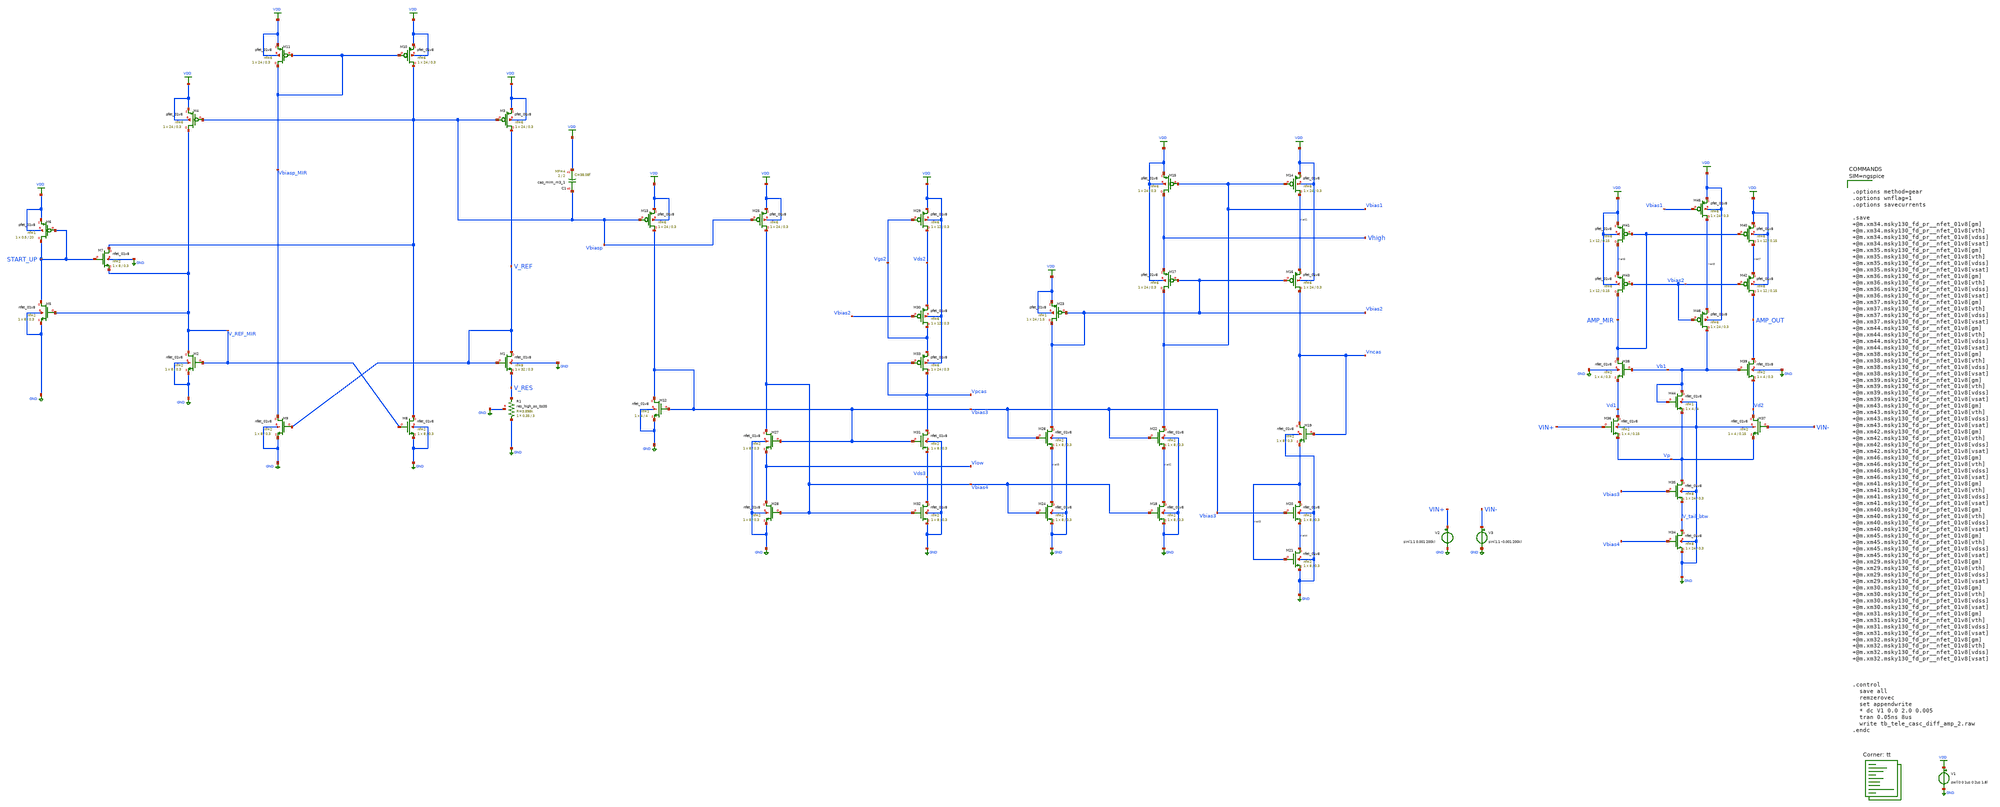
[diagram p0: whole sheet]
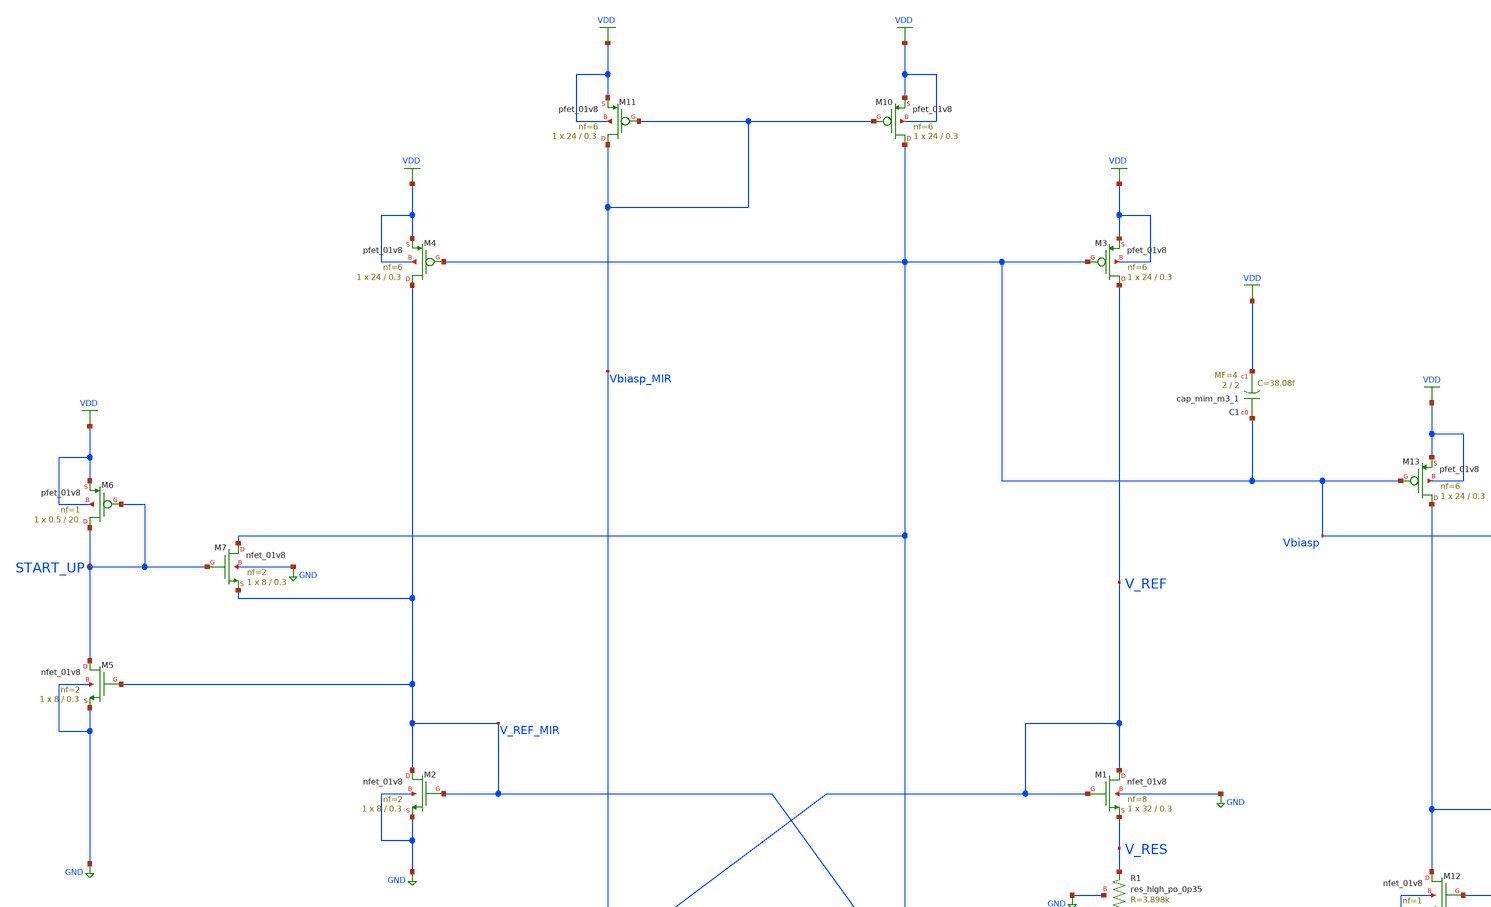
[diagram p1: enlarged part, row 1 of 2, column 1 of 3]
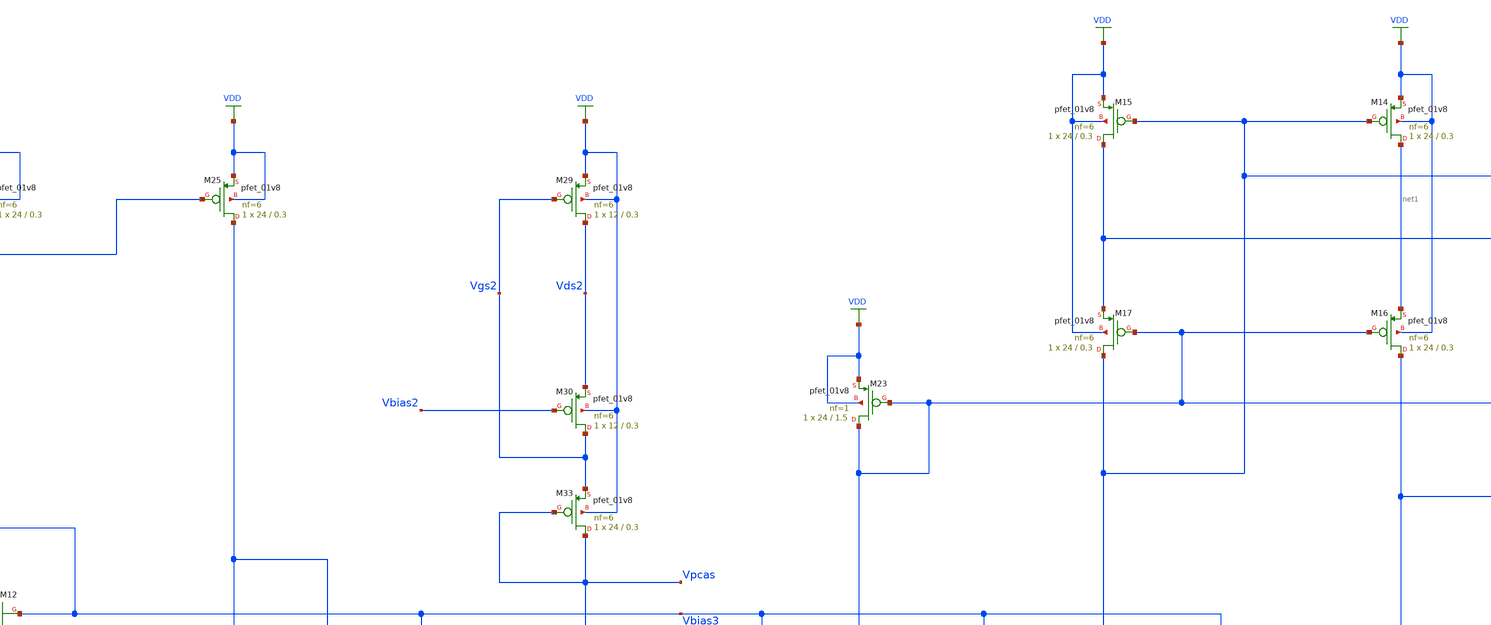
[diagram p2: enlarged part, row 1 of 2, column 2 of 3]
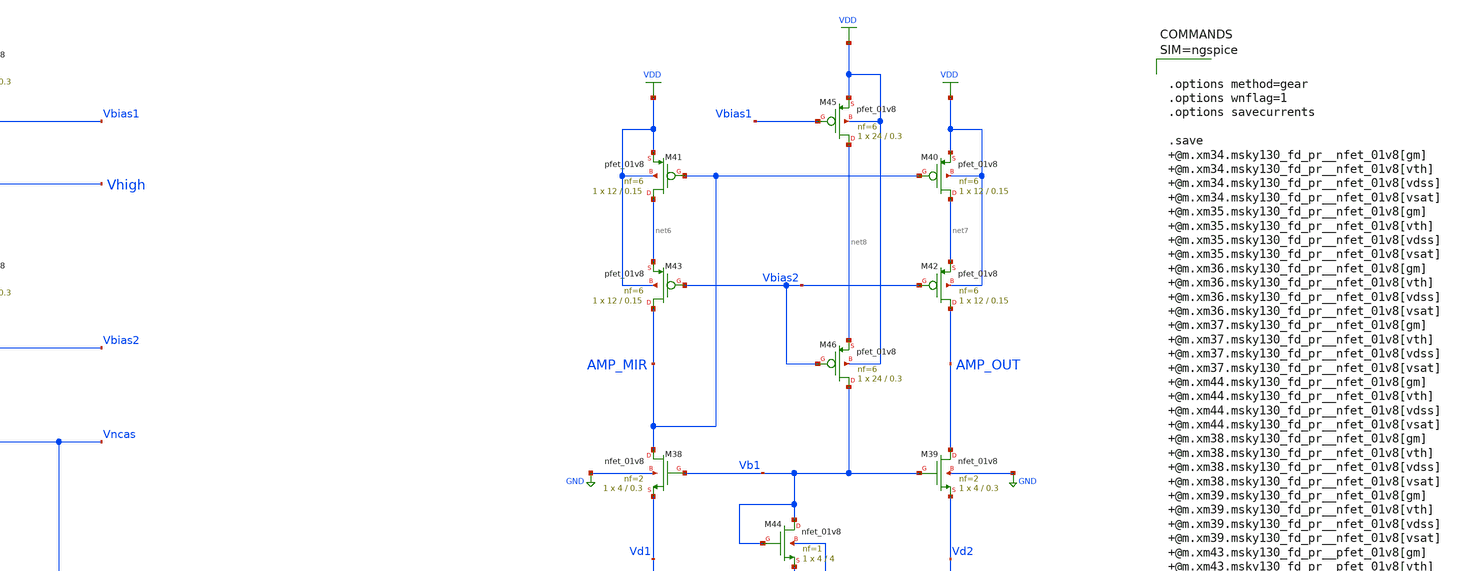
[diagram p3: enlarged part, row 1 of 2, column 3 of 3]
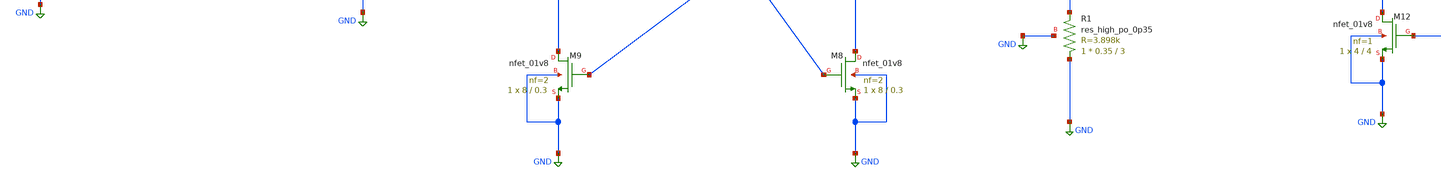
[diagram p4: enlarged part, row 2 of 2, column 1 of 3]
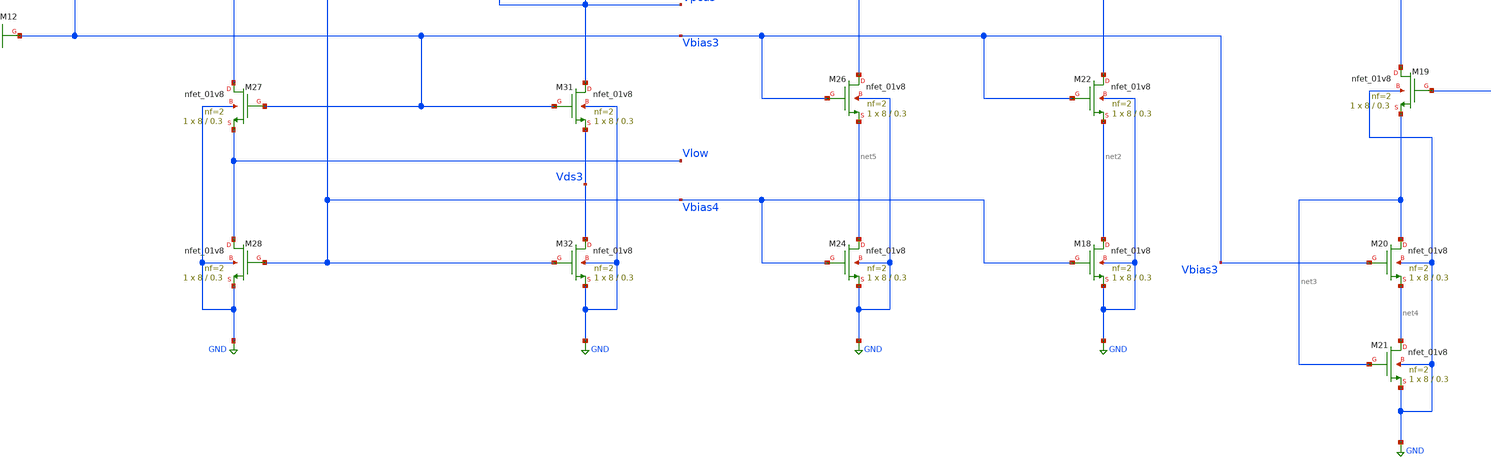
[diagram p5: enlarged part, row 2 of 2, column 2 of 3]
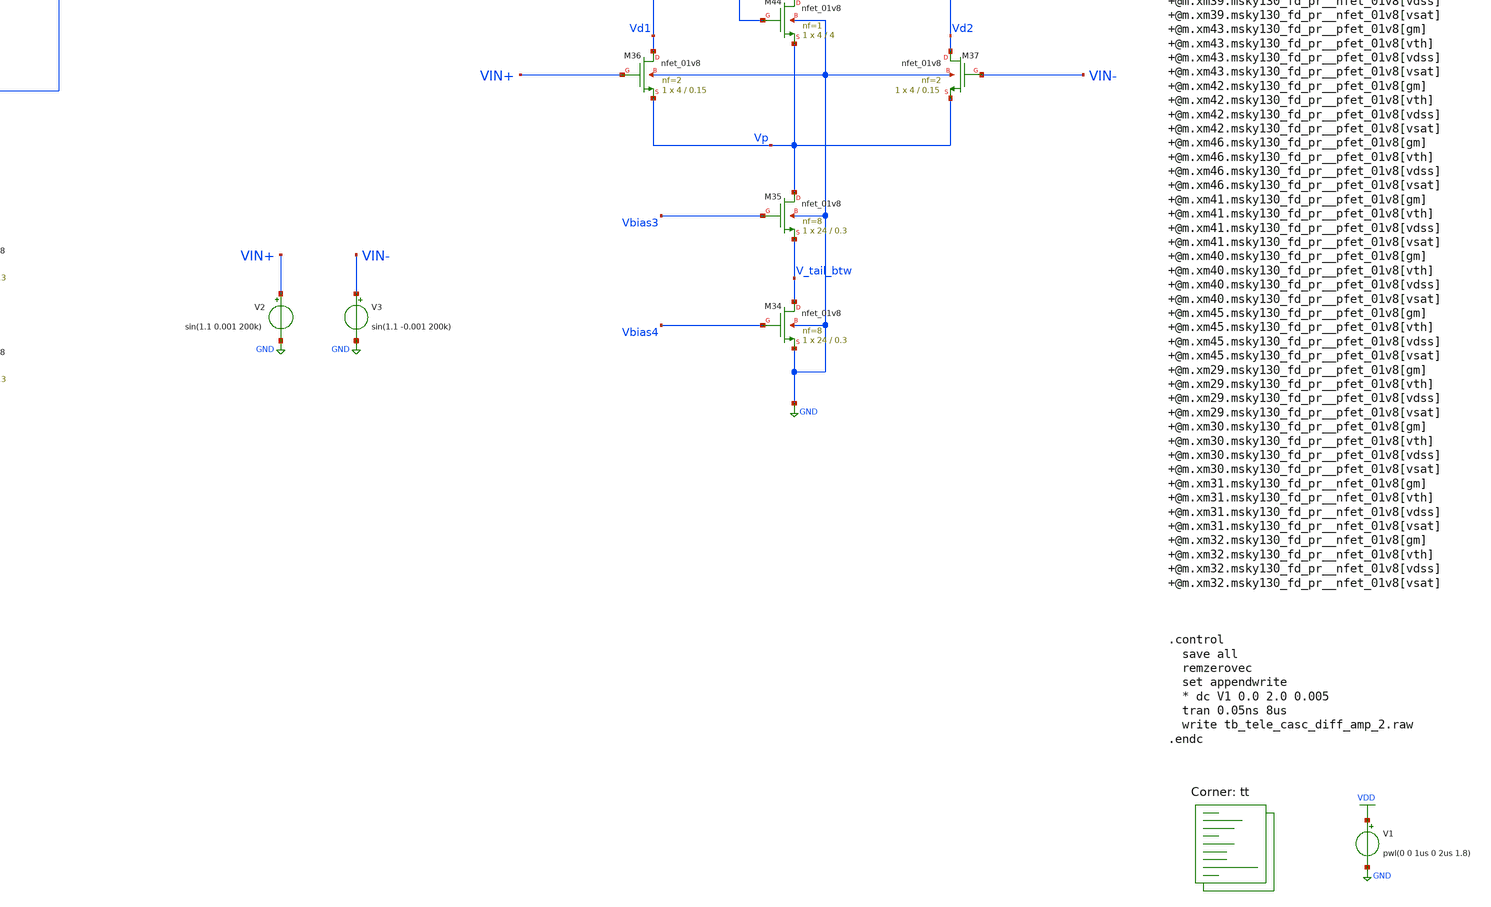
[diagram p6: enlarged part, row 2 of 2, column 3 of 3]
** sch_path: projects/ASU/EEE572/schematic/tb_tele_casc_diff_amp_2.sch
**.subckt tb_tele_casc_diff_amp_2
V1 VDD GND pwl(0 0 1us 0 2us 1.8)
XM1 V_REF V_REF V_RES GND sky130_fd_pr__nfet_01v8 L=0.3 W=32 nf=8 ad='int((nf+1)/2) * W/nf * 0.29' as='int((nf+2)/2) * W/nf * 0.29'
+ pd='2*int((nf+1)/2) * (W/nf + 0.29)' ps='2*int((nf+2)/2) * (W/nf + 0.29)' nrd='0.29 / W' nrs='0.29 / W'
+ sa=0 sb=0 sd=0 mult=1 m=1
XM2 V_REF_MIR V_REF_MIR GND GND sky130_fd_pr__nfet_01v8 L=0.3 W=8 nf=2 ad='int((nf+1)/2) * W/nf * 0.29'
+ as='int((nf+2)/2) * W/nf * 0.29' pd='2*int((nf+1)/2) * (W/nf + 0.29)' ps='2*int((nf+2)/2) * (W/nf + 0.29)'
+ nrd='0.29 / W' nrs='0.29 / W' sa=0 sb=0 sd=0 mult=1 m=1
XM5 START_UP V_REF_MIR GND GND sky130_fd_pr__nfet_01v8 L=0.3 W=8 nf=2 ad='int((nf+1)/2) * W/nf * 0.29'
+ as='int((nf+2)/2) * W/nf * 0.29' pd='2*int((nf+1)/2) * (W/nf + 0.29)' ps='2*int((nf+2)/2) * (W/nf + 0.29)'
+ nrd='0.29 / W' nrs='0.29 / W' sa=0 sb=0 sd=0 mult=1 m=1
XM7 Vbiasp START_UP V_REF_MIR GND sky130_fd_pr__nfet_01v8 L=0.3 W=8 nf=2 ad='int((nf+1)/2) * W/nf * 0.29'
+ as='int((nf+2)/2) * W/nf * 0.29' pd='2*int((nf+1)/2) * (W/nf + 0.29)' ps='2*int((nf+2)/2) * (W/nf + 0.29)'
+ nrd='0.29 / W' nrs='0.29 / W' sa=0 sb=0 sd=0 mult=1 m=1
XM6 START_UP START_UP VDD VDD sky130_fd_pr__pfet_01v8 L=20 W=0.5 nf=1 ad='int((nf+1)/2) * W/nf * 0.29'
+ as='int((nf+2)/2) * W/nf * 0.29' pd='2*int((nf+1)/2) * (W/nf + 0.29)' ps='2*int((nf+2)/2) * (W/nf + 0.29)'
+ nrd='0.29 / W' nrs='0.29 / W' sa=0 sb=0 sd=0 mult=1 m=1
XM3 V_REF Vbiasp VDD VDD sky130_fd_pr__pfet_01v8 L=0.3 W=24 nf=6 ad='int((nf+1)/2) * W/nf * 0.29' as='int((nf+2)/2) * W/nf * 0.29'
+ pd='2*int((nf+1)/2) * (W/nf + 0.29)' ps='2*int((nf+2)/2) * (W/nf + 0.29)' nrd='0.29 / W' nrs='0.29 / W'
+ sa=0 sb=0 sd=0 mult=1 m=1
XM4 V_REF_MIR Vbiasp VDD VDD sky130_fd_pr__pfet_01v8 L=0.3 W=24 nf=6 ad='int((nf+1)/2) * W/nf * 0.29'
+ as='int((nf+2)/2) * W/nf * 0.29' pd='2*int((nf+1)/2) * (W/nf + 0.29)' ps='2*int((nf+2)/2) * (W/nf + 0.29)'
+ nrd='0.29 / W' nrs='0.29 / W' sa=0 sb=0 sd=0 mult=1 m=1
XM8 Vbiasp V_REF_MIR GND GND sky130_fd_pr__nfet_01v8 L=0.3 W=8 nf=2 ad='int((nf+1)/2) * W/nf * 0.29'
+ as='int((nf+2)/2) * W/nf * 0.29' pd='2*int((nf+1)/2) * (W/nf + 0.29)' ps='2*int((nf+2)/2) * (W/nf + 0.29)'
+ nrd='0.29 / W' nrs='0.29 / W' sa=0 sb=0 sd=0 mult=1 m=1
XM9 Vbiasp_MIR V_REF GND GND sky130_fd_pr__nfet_01v8 L=0.3 W=8 nf=2 ad='int((nf+1)/2) * W/nf * 0.29'
+ as='int((nf+2)/2) * W/nf * 0.29' pd='2*int((nf+1)/2) * (W/nf + 0.29)' ps='2*int((nf+2)/2) * (W/nf + 0.29)'
+ nrd='0.29 / W' nrs='0.29 / W' sa=0 sb=0 sd=0 mult=1 m=1
XM10 Vbiasp Vbiasp_MIR VDD VDD sky130_fd_pr__pfet_01v8 L=0.3 W=24 nf=6 ad='int((nf+1)/2) * W/nf * 0.29'
+ as='int((nf+2)/2) * W/nf * 0.29' pd='2*int((nf+1)/2) * (W/nf + 0.29)' ps='2*int((nf+2)/2) * (W/nf + 0.29)'
+ nrd='0.29 / W' nrs='0.29 / W' sa=0 sb=0 sd=0 mult=1 m=1
XM11 Vbiasp_MIR Vbiasp_MIR VDD VDD sky130_fd_pr__pfet_01v8 L=0.3 W=24 nf=6 ad='int((nf+1)/2) * W/nf * 0.29'
+ as='int((nf+2)/2) * W/nf * 0.29' pd='2*int((nf+1)/2) * (W/nf + 0.29)' ps='2*int((nf+2)/2) * (W/nf + 0.29)'
+ nrd='0.29 / W' nrs='0.29 / W' sa=0 sb=0 sd=0 mult=1 m=1
XM12 Vbias3 Vbias3 GND GND sky130_fd_pr__nfet_01v8 L=4 W=4 nf=1 ad='int((nf+1)/2) * W/nf * 0.29' as='int((nf+2)/2) * W/nf * 0.29'
+ pd='2*int((nf+1)/2) * (W/nf + 0.29)' ps='2*int((nf+2)/2) * (W/nf + 0.29)' nrd='0.29 / W' nrs='0.29 / W'
+ sa=0 sb=0 sd=0 mult=1 m=1
XM13 Vbias3 Vbiasp VDD VDD sky130_fd_pr__pfet_01v8 L=0.3 W=24 nf=6 ad='int((nf+1)/2) * W/nf * 0.29' as='int((nf+2)/2) * W/nf * 0.29'
+ pd='2*int((nf+1)/2) * (W/nf + 0.29)' ps='2*int((nf+2)/2) * (W/nf + 0.29)' nrd='0.29 / W' nrs='0.29 / W'
+ sa=0 sb=0 sd=0 mult=1 m=1
XM14 net1 Vbias1 VDD VDD sky130_fd_pr__pfet_01v8 L=0.3 W=24 nf=6 ad='int((nf+1)/2) * W/nf * 0.29' as='int((nf+2)/2) * W/nf * 0.29'
+ pd='2*int((nf+1)/2) * (W/nf + 0.29)' ps='2*int((nf+2)/2) * (W/nf + 0.29)' nrd='0.29 / W' nrs='0.29 / W'
+ sa=0 sb=0 sd=0 mult=1 m=1
XM15 Vhigh Vbias1 VDD VDD sky130_fd_pr__pfet_01v8 L=0.3 W=24 nf=6 ad='int((nf+1)/2) * W/nf * 0.29' as='int((nf+2)/2) * W/nf * 0.29'
+ pd='2*int((nf+1)/2) * (W/nf + 0.29)' ps='2*int((nf+2)/2) * (W/nf + 0.29)' nrd='0.29 / W' nrs='0.29 / W'
+ sa=0 sb=0 sd=0 mult=1 m=1
XM16 Vncas Vbias2 net1 VDD sky130_fd_pr__pfet_01v8 L=0.3 W=24 nf=6 ad='int((nf+1)/2) * W/nf * 0.29' as='int((nf+2)/2) * W/nf * 0.29'
+ pd='2*int((nf+1)/2) * (W/nf + 0.29)' ps='2*int((nf+2)/2) * (W/nf + 0.29)' nrd='0.29 / W' nrs='0.29 / W'
+ sa=0 sb=0 sd=0 mult=1 m=1
XM17 Vbias1 Vbias2 Vhigh VDD sky130_fd_pr__pfet_01v8 L=0.3 W=24 nf=6 ad='int((nf+1)/2) * W/nf * 0.29'
+ as='int((nf+2)/2) * W/nf * 0.29' pd='2*int((nf+1)/2) * (W/nf + 0.29)' ps='2*int((nf+2)/2) * (W/nf + 0.29)'
+ nrd='0.29 / W' nrs='0.29 / W' sa=0 sb=0 sd=0 mult=1 m=1
XM18 net2 Vbias4 GND GND sky130_fd_pr__nfet_01v8 L=0.3 W=8 nf=2 ad='int((nf+1)/2) * W/nf * 0.29' as='int((nf+2)/2) * W/nf * 0.29'
+ pd='2*int((nf+1)/2) * (W/nf + 0.29)' ps='2*int((nf+2)/2) * (W/nf + 0.29)' nrd='0.29 / W' nrs='0.29 / W'
+ sa=0 sb=0 sd=0 mult=1 m=1
XM19 Vncas Vncas net3 GND sky130_fd_pr__nfet_01v8 L=0.3 W=8 nf=2 ad='int((nf+1)/2) * W/nf * 0.29' as='int((nf+2)/2) * W/nf * 0.29'
+ pd='2*int((nf+1)/2) * (W/nf + 0.29)' ps='2*int((nf+2)/2) * (W/nf + 0.29)' nrd='0.29 / W' nrs='0.29 / W'
+ sa=0 sb=0 sd=0 mult=1 m=1
XM20 net3 Vbias3 net4 GND sky130_fd_pr__nfet_01v8 L=0.3 W=8 nf=2 ad='int((nf+1)/2) * W/nf * 0.29' as='int((nf+2)/2) * W/nf * 0.29'
+ pd='2*int((nf+1)/2) * (W/nf + 0.29)' ps='2*int((nf+2)/2) * (W/nf + 0.29)' nrd='0.29 / W' nrs='0.29 / W'
+ sa=0 sb=0 sd=0 mult=1 m=1
XM21 net4 net3 GND GND sky130_fd_pr__nfet_01v8 L=0.3 W=8 nf=2 ad='int((nf+1)/2) * W/nf * 0.29' as='int((nf+2)/2) * W/nf * 0.29'
+ pd='2*int((nf+1)/2) * (W/nf + 0.29)' ps='2*int((nf+2)/2) * (W/nf + 0.29)' nrd='0.29 / W' nrs='0.29 / W'
+ sa=0 sb=0 sd=0 mult=1 m=1
XM25 Vbias4 Vbiasp VDD VDD sky130_fd_pr__pfet_01v8 L=0.3 W=24 nf=6 ad='int((nf+1)/2) * W/nf * 0.29' as='int((nf+2)/2) * W/nf * 0.29'
+ pd='2*int((nf+1)/2) * (W/nf + 0.29)' ps='2*int((nf+2)/2) * (W/nf + 0.29)' nrd='0.29 / W' nrs='0.29 / W'
+ sa=0 sb=0 sd=0 mult=1 m=1
XM27 Vbias4 Vbias3 Vlow GND sky130_fd_pr__nfet_01v8 L=0.3 W=8 nf=2 ad='int((nf+1)/2) * W/nf * 0.29' as='int((nf+2)/2) * W/nf * 0.29'
+ pd='2*int((nf+1)/2) * (W/nf + 0.29)' ps='2*int((nf+2)/2) * (W/nf + 0.29)' nrd='0.29 / W' nrs='0.29 / W'
+ sa=0 sb=0 sd=0 mult=1 m=1
XM28 Vlow Vbias4 GND GND sky130_fd_pr__nfet_01v8 L=0.3 W=8 nf=2 ad='int((nf+1)/2) * W/nf * 0.29' as='int((nf+2)/2) * W/nf * 0.29'
+ pd='2*int((nf+1)/2) * (W/nf + 0.29)' ps='2*int((nf+2)/2) * (W/nf + 0.29)' nrd='0.29 / W' nrs='0.29 / W'
+ sa=0 sb=0 sd=0 mult=1 m=1
XM29 Vds2 Vgs2 VDD VDD sky130_fd_pr__pfet_01v8 L=0.3 W=12 nf=6 ad='int((nf+1)/2) * W/nf * 0.29' as='int((nf+2)/2) * W/nf * 0.29'
+ pd='2*int((nf+1)/2) * (W/nf + 0.29)' ps='2*int((nf+2)/2) * (W/nf + 0.29)' nrd='0.29 / W' nrs='0.29 / W'
+ sa=0 sb=0 sd=0 mult=1 m=1
XM30 Vgs2 Vbias2 Vds2 VDD sky130_fd_pr__pfet_01v8 L=0.3 W=12 nf=6 ad='int((nf+1)/2) * W/nf * 0.29' as='int((nf+2)/2) * W/nf * 0.29'
+ pd='2*int((nf+1)/2) * (W/nf + 0.29)' ps='2*int((nf+2)/2) * (W/nf + 0.29)' nrd='0.29 / W' nrs='0.29 / W'
+ sa=0 sb=0 sd=0 mult=1 m=1
XM31 Vpcas Vbias3 Vds3 GND sky130_fd_pr__nfet_01v8 L=0.3 W=8 nf=2 ad='int((nf+1)/2) * W/nf * 0.29' as='int((nf+2)/2) * W/nf * 0.29'
+ pd='2*int((nf+1)/2) * (W/nf + 0.29)' ps='2*int((nf+2)/2) * (W/nf + 0.29)' nrd='0.29 / W' nrs='0.29 / W'
+ sa=0 sb=0 sd=0 mult=1 m=1
XM32 Vds3 Vbias4 GND GND sky130_fd_pr__nfet_01v8 L=0.3 W=8 nf=2 ad='int((nf+1)/2) * W/nf * 0.29' as='int((nf+2)/2) * W/nf * 0.29'
+ pd='2*int((nf+1)/2) * (W/nf + 0.29)' ps='2*int((nf+2)/2) * (W/nf + 0.29)' nrd='0.29 / W' nrs='0.29 / W'
+ sa=0 sb=0 sd=0 mult=1 m=1
XM33 Vpcas Vpcas Vgs2 VDD sky130_fd_pr__pfet_01v8 L=0.3 W=24 nf=6 ad='int((nf+1)/2) * W/nf * 0.29' as='int((nf+2)/2) * W/nf * 0.29'
+ pd='2*int((nf+1)/2) * (W/nf + 0.29)' ps='2*int((nf+2)/2) * (W/nf + 0.29)' nrd='0.29 / W' nrs='0.29 / W'
+ sa=0 sb=0 sd=0 mult=1 m=1
XM22 Vbias1 Vbias3 net2 GND sky130_fd_pr__nfet_01v8 L=0.3 W=8 nf=2 ad='int((nf+1)/2) * W/nf * 0.29' as='int((nf+2)/2) * W/nf * 0.29'
+ pd='2*int((nf+1)/2) * (W/nf + 0.29)' ps='2*int((nf+2)/2) * (W/nf + 0.29)' nrd='0.29 / W' nrs='0.29 / W'
+ sa=0 sb=0 sd=0 mult=1 m=1
XM23 Vbias2 Vbias2 VDD VDD sky130_fd_pr__pfet_01v8 L=1.5 W=24 nf=1 ad='int((nf+1)/2) * W/nf * 0.29' as='int((nf+2)/2) * W/nf * 0.29'
+ pd='2*int((nf+1)/2) * (W/nf + 0.29)' ps='2*int((nf+2)/2) * (W/nf + 0.29)' nrd='0.29 / W' nrs='0.29 / W'
+ sa=0 sb=0 sd=0 mult=1 m=1
XM24 net5 Vbias4 GND GND sky130_fd_pr__nfet_01v8 L=0.3 W=8 nf=2 ad='int((nf+1)/2) * W/nf * 0.29' as='int((nf+2)/2) * W/nf * 0.29'
+ pd='2*int((nf+1)/2) * (W/nf + 0.29)' ps='2*int((nf+2)/2) * (W/nf + 0.29)' nrd='0.29 / W' nrs='0.29 / W'
+ sa=0 sb=0 sd=0 mult=1 m=1
XM26 Vbias2 Vbias3 net5 GND sky130_fd_pr__nfet_01v8 L=0.3 W=8 nf=2 ad='int((nf+1)/2) * W/nf * 0.29' as='int((nf+2)/2) * W/nf * 0.29'
+ pd='2*int((nf+1)/2) * (W/nf + 0.29)' ps='2*int((nf+2)/2) * (W/nf + 0.29)' nrd='0.29 / W' nrs='0.29 / W'
+ sa=0 sb=0 sd=0 mult=1 m=1
XC1 Vbiasp VDD sky130_fd_pr__cap_mim_m3_1 W=2 L=2 MF=4 m=4
XM34 V_tail_btw Vbias4 GND GND sky130_fd_pr__nfet_01v8 L=0.3 W=24 nf=8 ad='int((nf+1)/2) * W/nf * 0.29'
+ as='int((nf+2)/2) * W/nf * 0.29' pd='2*int((nf+1)/2) * (W/nf + 0.29)' ps='2*int((nf+2)/2) * (W/nf + 0.29)'
+ nrd='0.29 / W' nrs='0.29 / W' sa=0 sb=0 sd=0 mult=1 m=1
XM35 Vp Vbias3 V_tail_btw GND sky130_fd_pr__nfet_01v8 L=0.3 W=24 nf=8 ad='int((nf+1)/2) * W/nf * 0.29'
+ as='int((nf+2)/2) * W/nf * 0.29' pd='2*int((nf+1)/2) * (W/nf + 0.29)' ps='2*int((nf+2)/2) * (W/nf + 0.29)'
+ nrd='0.29 / W' nrs='0.29 / W' sa=0 sb=0 sd=0 mult=1 m=1
XM36 Vd1 VIN+ Vp GND sky130_fd_pr__nfet_01v8 L=0.15 W=4 nf=2 ad='int((nf+1)/2) * W/nf * 0.29' as='int((nf+2)/2) * W/nf * 0.29'
+ pd='2*int((nf+1)/2) * (W/nf + 0.29)' ps='2*int((nf+2)/2) * (W/nf + 0.29)' nrd='0.29 / W' nrs='0.29 / W'
+ sa=0 sb=0 sd=0 mult=1 m=1
XM37 Vd2 VIN- Vp GND sky130_fd_pr__nfet_01v8 L=0.15 W=4 nf=2 ad='int((nf+1)/2) * W/nf * 0.29' as='int((nf+2)/2) * W/nf * 0.29'
+ pd='2*int((nf+1)/2) * (W/nf + 0.29)' ps='2*int((nf+2)/2) * (W/nf + 0.29)' nrd='0.29 / W' nrs='0.29 / W'
+ sa=0 sb=0 sd=0 mult=1 m=1
XM38 AMP_MIR Vb1 Vd1 GND sky130_fd_pr__nfet_01v8 L=0.3 W=4 nf=2 ad='int((nf+1)/2) * W/nf * 0.29' as='int((nf+2)/2) * W/nf * 0.29'
+ pd='2*int((nf+1)/2) * (W/nf + 0.29)' ps='2*int((nf+2)/2) * (W/nf + 0.29)' nrd='0.29 / W' nrs='0.29 / W'
+ sa=0 sb=0 sd=0 mult=1 m=1
XM39 AMP_OUT Vb1 Vd2 GND sky130_fd_pr__nfet_01v8 L=0.3 W=4 nf=2 ad='int((nf+1)/2) * W/nf * 0.29' as='int((nf+2)/2) * W/nf * 0.29'
+ pd='2*int((nf+1)/2) * (W/nf + 0.29)' ps='2*int((nf+2)/2) * (W/nf + 0.29)' nrd='0.29 / W' nrs='0.29 / W'
+ sa=0 sb=0 sd=0 mult=1 m=1
XM40 net7 AMP_MIR VDD VDD sky130_fd_pr__pfet_01v8 L=0.15 W=12 nf=6 ad='int((nf+1)/2) * W/nf * 0.29' as='int((nf+2)/2) * W/nf * 0.29'
+ pd='2*int((nf+1)/2) * (W/nf + 0.29)' ps='2*int((nf+2)/2) * (W/nf + 0.29)' nrd='0.29 / W' nrs='0.29 / W'
+ sa=0 sb=0 sd=0 mult=1 m=1
XM41 net6 AMP_MIR VDD VDD sky130_fd_pr__pfet_01v8 L=0.15 W=12 nf=6 ad='int((nf+1)/2) * W/nf * 0.29' as='int((nf+2)/2) * W/nf * 0.29'
+ pd='2*int((nf+1)/2) * (W/nf + 0.29)' ps='2*int((nf+2)/2) * (W/nf + 0.29)' nrd='0.29 / W' nrs='0.29 / W'
+ sa=0 sb=0 sd=0 mult=1 m=1
XM42 AMP_OUT Vbias2 net7 VDD sky130_fd_pr__pfet_01v8 L=0.15 W=12 nf=6 ad='int((nf+1)/2) * W/nf * 0.29'
+ as='int((nf+2)/2) * W/nf * 0.29' pd='2*int((nf+1)/2) * (W/nf + 0.29)' ps='2*int((nf+2)/2) * (W/nf + 0.29)'
+ nrd='0.29 / W' nrs='0.29 / W' sa=0 sb=0 sd=0 mult=1 m=1
XM43 AMP_MIR Vbias2 net6 VDD sky130_fd_pr__pfet_01v8 L=0.15 W=12 nf=6 ad='int((nf+1)/2) * W/nf * 0.29'
+ as='int((nf+2)/2) * W/nf * 0.29' pd='2*int((nf+1)/2) * (W/nf + 0.29)' ps='2*int((nf+2)/2) * (W/nf + 0.29)'
+ nrd='0.29 / W' nrs='0.29 / W' sa=0 sb=0 sd=0 mult=1 m=1
XM44 Vb1 Vb1 Vp GND sky130_fd_pr__nfet_01v8 L=4 W=4 nf=1 ad='int((nf+1)/2) * W/nf * 0.29' as='int((nf+2)/2) * W/nf * 0.29'
+ pd='2*int((nf+1)/2) * (W/nf + 0.29)' ps='2*int((nf+2)/2) * (W/nf + 0.29)' nrd='0.29 / W' nrs='0.29 / W'
+ sa=0 sb=0 sd=0 mult=1 m=1
XM45 net8 Vbias1 VDD VDD sky130_fd_pr__pfet_01v8 L=0.3 W=24 nf=6 ad='int((nf+1)/2) * W/nf * 0.29' as='int((nf+2)/2) * W/nf * 0.29'
+ pd='2*int((nf+1)/2) * (W/nf + 0.29)' ps='2*int((nf+2)/2) * (W/nf + 0.29)' nrd='0.29 / W' nrs='0.29 / W'
+ sa=0 sb=0 sd=0 mult=1 m=1
XM46 Vb1 Vbias2 net8 VDD sky130_fd_pr__pfet_01v8 L=0.3 W=24 nf=6 ad='int((nf+1)/2) * W/nf * 0.29' as='int((nf+2)/2) * W/nf * 0.29'
+ pd='2*int((nf+1)/2) * (W/nf + 0.29)' ps='2*int((nf+2)/2) * (W/nf + 0.29)' nrd='0.29 / W' nrs='0.29 / W'
+ sa=0 sb=0 sd=0 mult=1 m=1
V3 VIN- GND sin(1.1 -0.001 200k)
V2 VIN+ GND sin(1.1 0.001 200k)
XR1 GND V_RES GND sky130_fd_pr__res_high_po_0p35 L=3 mult=1 m=1
**** begin user architecture code
.lib $::SKYWATER_MODELS/sky130.lib.spice tt



.options method=gear
.options wnflag=1
.options savecurrents

.save @m.xm34.msky130_fd_pr__nfet_01v8[gm] @m.xm34.msky130_fd_pr__nfet_01v8[vth] @m.xm34.msky130_fd_pr__nfet_01v8[vdss] @m.xm34.msky130_fd_pr__nfet_01v8[vsat] @m.xm35.msky130_fd_pr__nfet_01v8[gm] @m.xm35.msky130_fd_pr__nfet_01v8[vth] @m.xm35.msky130_fd_pr__nfet_01v8[vdss] @m.xm35.msky130_fd_pr__nfet_01v8[vsat] @m.xm36.msky130_fd_pr__nfet_01v8[gm] @m.xm36.msky130_fd_pr__nfet_01v8[vth] @m.xm36.msky130_fd_pr__nfet_01v8[vdss] @m.xm36.msky130_fd_pr__nfet_01v8[vsat] @m.xm37.msky130_fd_pr__nfet_01v8[gm] @m.xm37.msky130_fd_pr__nfet_01v8[vth] @m.xm37.msky130_fd_pr__nfet_01v8[vdss] @m.xm37.msky130_fd_pr__nfet_01v8[vsat] @m.xm44.msky130_fd_pr__nfet_01v8[gm] @m.xm44.msky130_fd_pr__nfet_01v8[vth] @m.xm44.msky130_fd_pr__nfet_01v8[vdss] @m.xm44.msky130_fd_pr__nfet_01v8[vsat] @m.xm38.msky130_fd_pr__nfet_01v8[gm] @m.xm38.msky130_fd_pr__nfet_01v8[vth] @m.xm38.msky130_fd_pr__nfet_01v8[vdss] @m.xm38.msky130_fd_pr__nfet_01v8[vsat] @m.xm39.msky130_fd_pr__nfet_01v8[gm] @m.xm39.msky130_fd_pr__nfet_01v8[vth] @m.xm39.msky130_fd_pr__nfet_01v8[vdss] @m.xm39.msky130_fd_pr__nfet_01v8[vsat] @m.xm43.msky130_fd_pr__pfet_01v8[gm] @m.xm43.msky130_fd_pr__pfet_01v8[vth] @m.xm43.msky130_fd_pr__pfet_01v8[vdss] @m.xm43.msky130_fd_pr__pfet_01v8[vsat] @m.xm42.msky130_fd_pr__pfet_01v8[gm] @m.xm42.msky130_fd_pr__pfet_01v8[vth] @m.xm42.msky130_fd_pr__pfet_01v8[vdss] @m.xm42.msky130_fd_pr__pfet_01v8[vsat] @m.xm46.msky130_fd_pr__pfet_01v8[gm] @m.xm46.msky130_fd_pr__pfet_01v8[vth] @m.xm46.msky130_fd_pr__pfet_01v8[vdss] @m.xm46.msky130_fd_pr__pfet_01v8[vsat] @m.xm41.msky130_fd_pr__pfet_01v8[gm] @m.xm41.msky130_fd_pr__pfet_01v8[vth] @m.xm41.msky130_fd_pr__pfet_01v8[vdss] @m.xm41.msky130_fd_pr__pfet_01v8[vsat] @m.xm40.msky130_fd_pr__pfet_01v8[gm] @m.xm40.msky130_fd_pr__pfet_01v8[vth] @m.xm40.msky130_fd_pr__pfet_01v8[vdss] @m.xm40.msky130_fd_pr__pfet_01v8[vsat] @m.xm45.msky130_fd_pr__pfet_01v8[gm] @m.xm45.msky130_fd_pr__pfet_01v8[vth] @m.xm45.msky130_fd_pr__pfet_01v8[vdss] @m.xm45.msky130_fd_pr__pfet_01v8[vsat] @m.xm29.msky130_fd_pr__pfet_01v8[gm] @m.xm29.msky130_fd_pr__pfet_01v8[vth] @m.xm29.msky130_fd_pr__pfet_01v8[vdss] @m.xm29.msky130_fd_pr__pfet_01v8[vsat] @m.xm30.msky130_fd_pr__pfet_01v8[gm] @m.xm30.msky130_fd_pr__pfet_01v8[vth] @m.xm30.msky130_fd_pr__pfet_01v8[vdss] @m.xm30.msky130_fd_pr__pfet_01v8[vsat] @m.xm31.msky130_fd_pr__nfet_01v8[gm] @m.xm31.msky130_fd_pr__nfet_01v8[vth] @m.xm31.msky130_fd_pr__nfet_01v8[vdss] @m.xm31.msky130_fd_pr__nfet_01v8[vsat] @m.xm32.msky130_fd_pr__nfet_01v8[gm] @m.xm32.msky130_fd_pr__nfet_01v8[vth] @m.xm32.msky130_fd_pr__nfet_01v8[vdss] @m.xm32.msky130_fd_pr__nfet_01v8[vsat]



.control
  save all
  remzerovec
  set appendwrite
  * dc V1 0.0 2.0 0.005
  tran 0.05ns 8us
  write tb_tele_casc_diff_amp_2.raw
.endc





**** end user architecture code
**.ends
.GLOBAL GND
.GLOBAL VDD
.end
